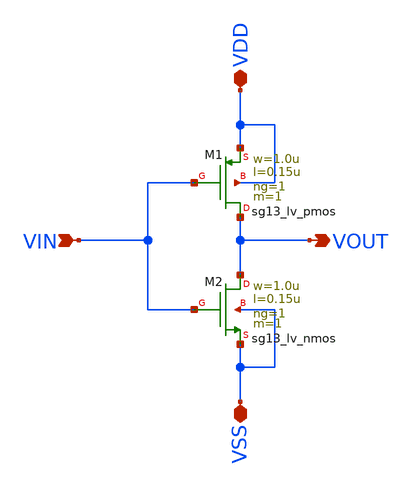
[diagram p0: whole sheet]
** sch_path: Taller2_extendido/Insumos/Simbolo_Support_1.sch
**.subckt Simbolo_Support_1 VIN VDD VSS VOUT
*.ipin VIN
*.iopin VDD
*.iopin VSS
*.opin VOUT
XM1 VOUT VIN VDD VDD sg13_lv_pmos w=1.0u l=0.15u ng=1 m=1 mm_ok=1
XM2 VOUT VIN VSS VSS sg13_lv_nmos w=1.0u l=0.15u ng=1 m=1 mm_ok=1
**.ends
.end
